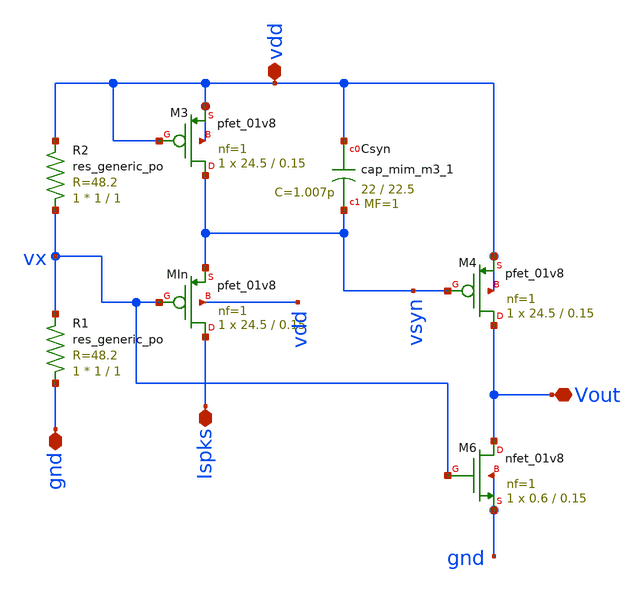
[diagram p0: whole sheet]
** sch_path: Neuron/ultralif/integrator.sch
**.subckt integrator Ispks Vout vdd gnd
*.iopin Ispks
*.iopin Vout
*.iopin vdd
*.iopin gnd
XMIn Ispks vx vsyn vdd sky130_fd_pr__pfet_01v8 L=0.15 W=24.5 nf=1 ad='int((nf+1)/2) * W/nf * 0.29' as='int((nf+2)/2) * W/nf * 0.29'
+ pd='2*int((nf+1)/2) * (W/nf + 0.29)' ps='2*int((nf+2)/2) * (W/nf + 0.29)' nrd='0.29 / W' nrs='0.29 / W'
+ sa=0 sb=0 sd=0 mult=1 m=1
XM3 vsyn vdd vdd vdd sky130_fd_pr__pfet_01v8 L=0.15 W=24.5 nf=1 ad='int((nf+1)/2) * W/nf * 0.29' as='int((nf+2)/2) * W/nf * 0.29'
+ pd='2*int((nf+1)/2) * (W/nf + 0.29)' ps='2*int((nf+2)/2) * (W/nf + 0.29)' nrd='0.29 / W' nrs='0.29 / W'
+ sa=0 sb=0 sd=0 mult=1 m=1
XM4 Vout vsyn vdd vdd sky130_fd_pr__pfet_01v8 L=0.15 W=24.5 nf=1 ad='int((nf+1)/2) * W/nf * 0.29' as='int((nf+2)/2) * W/nf * 0.29'
+ pd='2*int((nf+1)/2) * (W/nf + 0.29)' ps='2*int((nf+2)/2) * (W/nf + 0.29)' nrd='0.29 / W' nrs='0.29 / W'
+ sa=0 sb=0 sd=0 mult=1 m=1
XCsyn vdd vsyn sky130_fd_pr__cap_mim_m3_1 W=22 L=22.5 MF=1 m=1
XR2 vx vdd sky130_fd_pr__res_generic_po W=1 L=1 m=1
XR1 gnd vx sky130_fd_pr__res_generic_po W=1 L=1 m=1
XM6 Vout vx gnd gnd sky130_fd_pr__nfet_01v8 L=0.15 W=0.6 nf=1 ad='int((nf+1)/2) * W/nf * 0.29' as='int((nf+2)/2) * W/nf * 0.29'
+ pd='2*int((nf+1)/2) * (W/nf + 0.29)' ps='2*int((nf+2)/2) * (W/nf + 0.29)' nrd='0.29 / W' nrs='0.29 / W'
+ sa=0 sb=0 sd=0 mult=1 m=1
**.ends
.end
